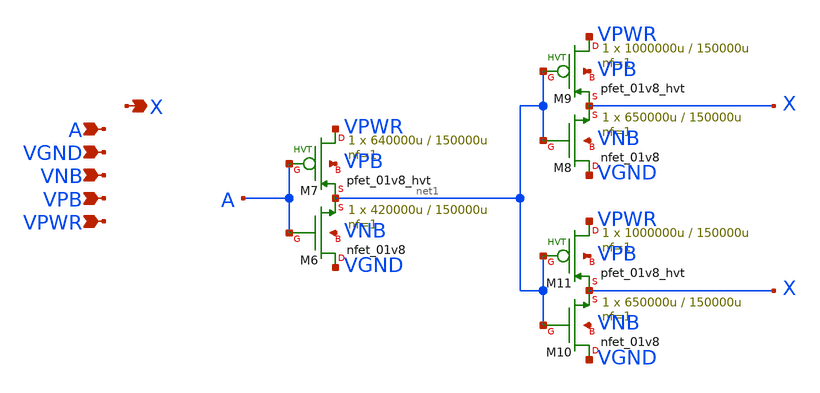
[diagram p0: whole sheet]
** sch_path: schematics/buf/sky130_fd_sc_hd__buf_2.sch
**.subckt sky130_fd_sc_hd__buf_2 A VGND VNB VPB VPWR X
*.ipin A
*.ipin VGND
*.ipin VNB
*.ipin VPB
*.ipin VPWR
*.opin X
XM6 VGND A net1 VNB sky130_fd_pr__nfet_01v8 L=150000u W=420000u nf=1 ad='int((1 + 1)/2) * 420000u / 1 * 0.29'
+ as='int((1 + 2)/2) * 420000u / 1 * 0.29' pd='2*int((1 + 1)/2) * (420000u / 1 + 0.29)' ps='2*int((1 + 2)/2) * (420000u / 1 + 0.29)'
+ nrd='0.29 / 420000u ' nrs='0.29 / 420000u ' sa=0 sb=0 sd=0 mult=1 m=1
XM7 VPWR A net1 VPB sky130_fd_pr__pfet_01v8_hvt L=150000u W=640000u nf=1 ad='int((1 + 1)/2) * 640000u / 1 * 0.29'
+ as='int((1 + 2)/2) * 640000u / 1 * 0.29' pd='2*int((1 + 1)/2) * (640000u / 1 + 0.29)' ps='2*int((1 + 2)/2) * (640000u / 1 + 0.29)'
+ nrd='0.29 / 640000u ' nrs='0.29 / 640000u ' sa=0 sb=0 sd=0 mult=1 m=1
XM8 VGND net1 X VNB sky130_fd_pr__nfet_01v8 L=150000u W=650000u nf=1 ad='int((1 + 1)/2) * 650000u / 1 * 0.29'
+ as='int((1 + 2)/2) * 650000u / 1 * 0.29' pd='2*int((1 + 1)/2) * (650000u / 1 + 0.29)' ps='2*int((1 + 2)/2) * (650000u / 1 + 0.29)'
+ nrd='0.29 / 650000u ' nrs='0.29 / 650000u ' sa=0 sb=0 sd=0 mult=1 m=1
XM9 VPWR net1 X VPB sky130_fd_pr__pfet_01v8_hvt L=150000u W=1000000u nf=1 ad='int((1 + 1)/2) * 1000000u / 1 * 0.29'
+ as='int((1 + 2)/2) * 1000000u / 1 * 0.29' pd='2*int((1 + 1)/2) * (1000000u / 1 + 0.29)' ps='2*int((1 + 2)/2) * (1000000u / 1 + 0.29)'
+ nrd='0.29 / 1000000u ' nrs='0.29 / 1000000u ' sa=0 sb=0 sd=0 mult=1 m=1
XM10 VGND net1 X VNB sky130_fd_pr__nfet_01v8 L=150000u W=650000u nf=1 ad='int((1 + 1)/2) * 650000u / 1 * 0.29'
+ as='int((1 + 2)/2) * 650000u / 1 * 0.29' pd='2*int((1 + 1)/2) * (650000u / 1 + 0.29)' ps='2*int((1 + 2)/2) * (650000u / 1 + 0.29)'
+ nrd='0.29 / 650000u ' nrs='0.29 / 650000u ' sa=0 sb=0 sd=0 mult=1 m=1
XM11 VPWR net1 X VPB sky130_fd_pr__pfet_01v8_hvt L=150000u W=1000000u nf=1 ad='int((1 + 1)/2) * 1000000u / 1 * 0.29'
+ as='int((1 + 2)/2) * 1000000u / 1 * 0.29' pd='2*int((1 + 1)/2) * (1000000u / 1 + 0.29)' ps='2*int((1 + 2)/2) * (1000000u / 1 + 0.29)'
+ nrd='0.29 / 1000000u ' nrs='0.29 / 1000000u ' sa=0 sb=0 sd=0 mult=1 m=1
**.ends
.end
